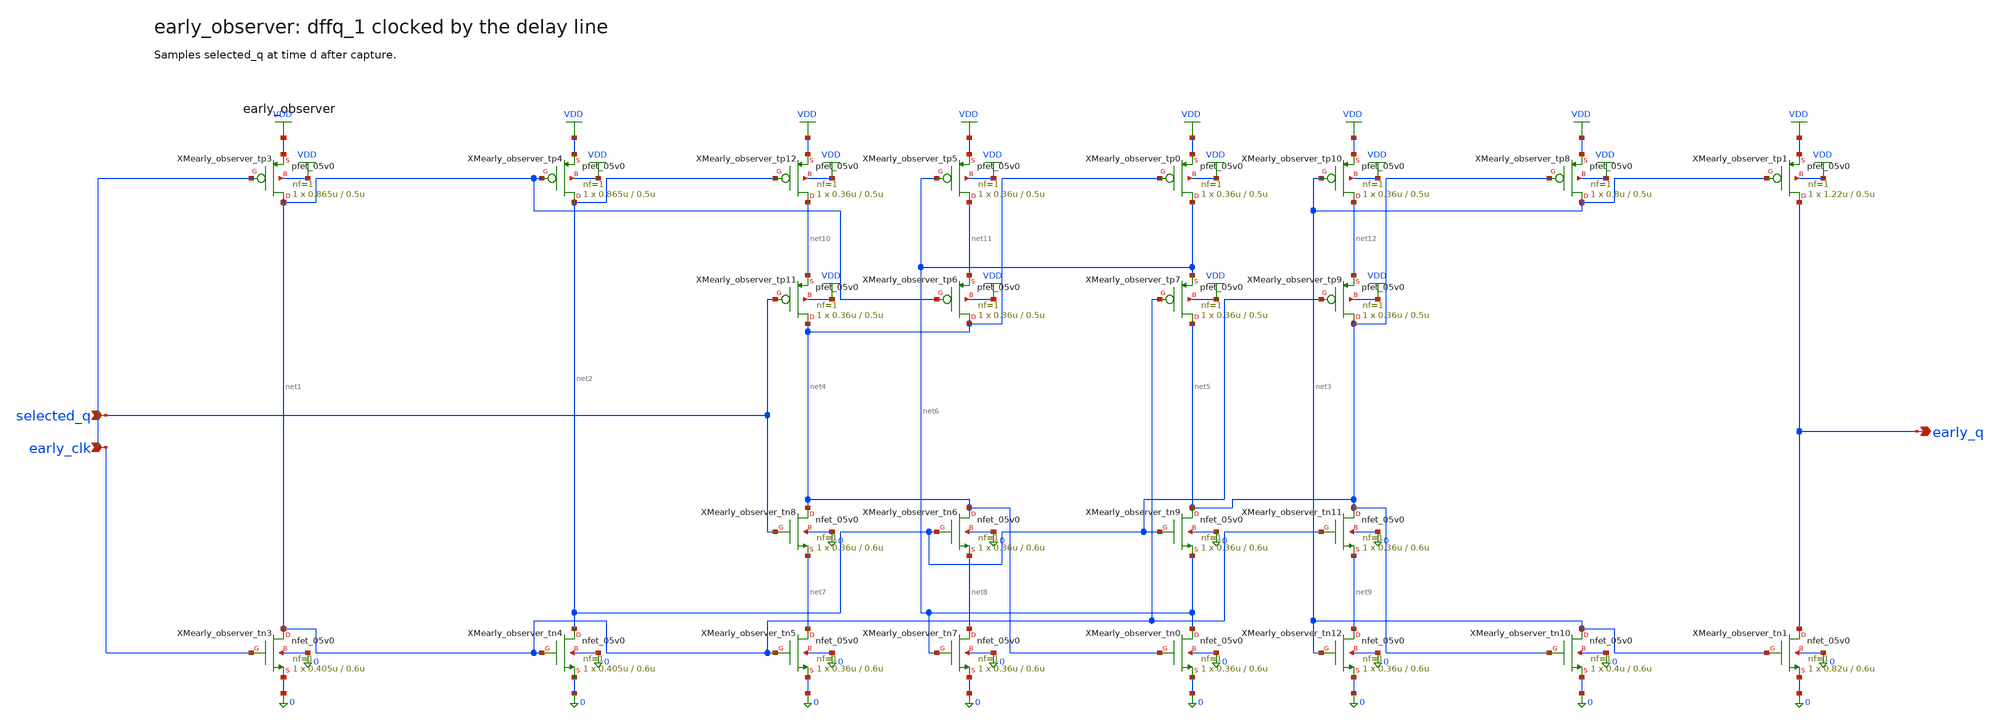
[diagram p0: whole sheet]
** sch_path: xschem/flat/early_observer.sch
**.subckt early_observer selected_q early_clk early_q
*.ipin selected_q
*.ipin early_clk
*.opin early_q
XMearly_observer_tn3 net1 early_clk 0 0 nfet_05v0 L=0.6u W=0.405u nf=1 ad=2.025e-13 as=2.025e-13
+ pd=1.81e-06 ps=1.81e-06 nrd=0 nrs=0 sa=0 sb=0 sd=0 m=1
XMearly_observer_tn4 net2 net1 0 0 nfet_05v0 L=0.6u W=0.405u nf=1 ad=2.025e-13 as=2.025e-13
+ pd=1.81e-06 ps=1.81e-06 nrd=0 nrs=0 sa=0 sb=0 sd=0 m=1
XMearly_observer_tn5 net7 net1 0 0 nfet_05v0 L=0.6u W=0.36u nf=1 ad=1.8e-13 as=1.8e-13 pd=1.72e-06
+ ps=1.72e-06 nrd=0 nrs=0 sa=0 sb=0 sd=0 m=1
XMearly_observer_tn8 net4 selected_q net7 0 nfet_05v0 L=0.6u W=0.36u nf=1 ad=1.8e-13 as=1.8e-13
+ pd=1.72e-06 ps=1.72e-06 nrd=0 nrs=0 sa=0 sb=0 sd=0 m=1
XMearly_observer_tn6 net4 net2 net8 0 nfet_05v0 L=0.6u W=0.36u nf=1 ad=1.8e-13 as=1.8e-13
+ pd=1.72e-06 ps=1.72e-06 nrd=0 nrs=0 sa=0 sb=0 sd=0 m=1
XMearly_observer_tn7 net8 net6 0 0 nfet_05v0 L=0.6u W=0.36u nf=1 ad=1.8e-13 as=1.8e-13 pd=1.72e-06
+ ps=1.72e-06 nrd=0 nrs=0 sa=0 sb=0 sd=0 m=1
XMearly_observer_tn0 net6 net4 0 0 nfet_05v0 L=0.6u W=0.36u nf=1 ad=1.8e-13 as=1.8e-13 pd=1.72e-06
+ ps=1.72e-06 nrd=0 nrs=0 sa=0 sb=0 sd=0 m=1
XMearly_observer_tn9 net5 net2 net6 0 nfet_05v0 L=0.6u W=0.36u nf=1 ad=1.8e-13 as=1.8e-13
+ pd=1.72e-06 ps=1.72e-06 nrd=0 nrs=0 sa=0 sb=0 sd=0 m=1
XMearly_observer_tn11 net5 net1 net9 0 nfet_05v0 L=0.6u W=0.36u nf=1 ad=1.8e-13 as=1.8e-13
+ pd=1.72e-06 ps=1.72e-06 nrd=0 nrs=0 sa=0 sb=0 sd=0 m=1
XMearly_observer_tn12 net9 net3 0 0 nfet_05v0 L=0.6u W=0.36u nf=1 ad=1.8e-13 as=1.8e-13 pd=1.72e-06
+ ps=1.72e-06 nrd=0 nrs=0 sa=0 sb=0 sd=0 m=1
XMearly_observer_tn10 net3 net5 0 0 nfet_05v0 L=0.6u W=0.4u nf=1 ad=2e-13 as=2e-13 pd=1.8e-06
+ ps=1.8e-06 nrd=0 nrs=0 sa=0 sb=0 sd=0 m=1
XMearly_observer_tn1 early_q net3 0 0 nfet_05v0 L=0.6u W=0.82u nf=1 ad=4.1e-13 as=4.1e-13
+ pd=2.64e-06 ps=2.64e-06 nrd=0 nrs=0 sa=0 sb=0 sd=0 m=1
XMearly_observer_tp3 net1 early_clk VDD VDD pfet_05v0 L=0.5u W=0.865u nf=1 ad=4.325e-13 as=4.325e-13
+ pd=2.73e-06 ps=2.73e-06 nrd=0 nrs=0 sa=0 sb=0 sd=0 m=1
XMearly_observer_tp4 net2 net1 VDD VDD pfet_05v0 L=0.5u W=0.865u nf=1 ad=4.325e-13 as=4.325e-13
+ pd=2.73e-06 ps=2.73e-06 nrd=0 nrs=0 sa=0 sb=0 sd=0 m=1
XMearly_observer_tp12 net10 net2 VDD VDD pfet_05v0 L=0.5u W=0.36u nf=1 ad=1.8e-13 as=1.8e-13
+ pd=1.72e-06 ps=1.72e-06 nrd=0 nrs=0 sa=0 sb=0 sd=0 m=1
XMearly_observer_tp11 net4 selected_q net10 VDD pfet_05v0 L=0.5u W=0.36u nf=1 ad=1.8e-13 as=1.8e-13
+ pd=1.72e-06 ps=1.72e-06 nrd=0 nrs=0 sa=0 sb=0 sd=0 m=1
XMearly_observer_tp6 net4 net1 net11 VDD pfet_05v0 L=0.5u W=0.36u nf=1 ad=1.8e-13 as=1.8e-13
+ pd=1.72e-06 ps=1.72e-06 nrd=0 nrs=0 sa=0 sb=0 sd=0 m=1
XMearly_observer_tp5 net11 net6 VDD VDD pfet_05v0 L=0.5u W=0.36u nf=1 ad=1.8e-13 as=1.8e-13
+ pd=1.72e-06 ps=1.72e-06 nrd=0 nrs=0 sa=0 sb=0 sd=0 m=1
XMearly_observer_tp0 net6 net4 VDD VDD pfet_05v0 L=0.5u W=0.36u nf=1 ad=1.8e-13 as=1.8e-13
+ pd=1.72e-06 ps=1.72e-06 nrd=0 nrs=0 sa=0 sb=0 sd=0 m=1
XMearly_observer_tp7 net5 net1 net6 VDD pfet_05v0 L=0.5u W=0.36u nf=1 ad=1.8e-13 as=1.8e-13
+ pd=1.72e-06 ps=1.72e-06 nrd=0 nrs=0 sa=0 sb=0 sd=0 m=1
XMearly_observer_tp9 net5 net2 net12 VDD pfet_05v0 L=0.5u W=0.36u nf=1 ad=1.8e-13 as=1.8e-13
+ pd=1.72e-06 ps=1.72e-06 nrd=0 nrs=0 sa=0 sb=0 sd=0 m=1
XMearly_observer_tp10 net12 net3 VDD VDD pfet_05v0 L=0.5u W=0.36u nf=1 ad=1.8e-13 as=1.8e-13
+ pd=1.72e-06 ps=1.72e-06 nrd=0 nrs=0 sa=0 sb=0 sd=0 m=1
XMearly_observer_tp8 net3 net5 VDD VDD pfet_05v0 L=0.5u W=0.8u nf=1 ad=4e-13 as=4e-13 pd=2.6e-06
+ ps=2.6e-06 nrd=0 nrs=0 sa=0 sb=0 sd=0 m=1
XMearly_observer_tp1 early_q net3 VDD VDD pfet_05v0 L=0.5u W=1.22u nf=1 ad=6.1e-13 as=6.1e-13
+ pd=3.44e-06 ps=3.44e-06 nrd=0 nrs=0 sa=0 sb=0 sd=0 m=1
**.ends
.GLOBAL VDD
.end
